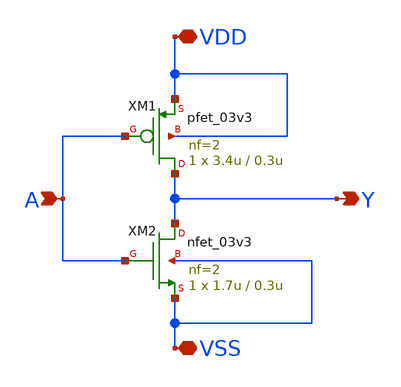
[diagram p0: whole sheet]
** sch_path: xschem/inv.sch
**.subckt inv A VDD VSS Y
*.ipin A
*.iopin VDD
*.iopin VSS
*.opin Y
XM1 Y A VDD VDD pfet_03v3 L=0.3u W=3.4u nf=2 ad='int((nf+1)/2) * W/nf * 0.18u' as='int((nf+2)/2) * W/nf * 0.18u'
+ pd='2*int((nf+1)/2) * (W/nf + 0.18u)' ps='2*int((nf+2)/2) * (W/nf + 0.18u)' nrd='0.18u / W' nrs='0.18u / W'
+ sa=0 sb=0 sd=0 m=1
XM2 Y A VSS VSS nfet_03v3 L=0.3u W=1.7u nf=2 ad='int((nf+1)/2) * W/nf * 0.18u' as='int((nf+2)/2) * W/nf * 0.18u'
+ pd='2*int((nf+1)/2) * (W/nf + 0.18u)' ps='2*int((nf+2)/2) * (W/nf + 0.18u)' nrd='0.18u / W' nrs='0.18u / W'
+ sa=0 sb=0 sd=0 m=1
**.ends
.end
